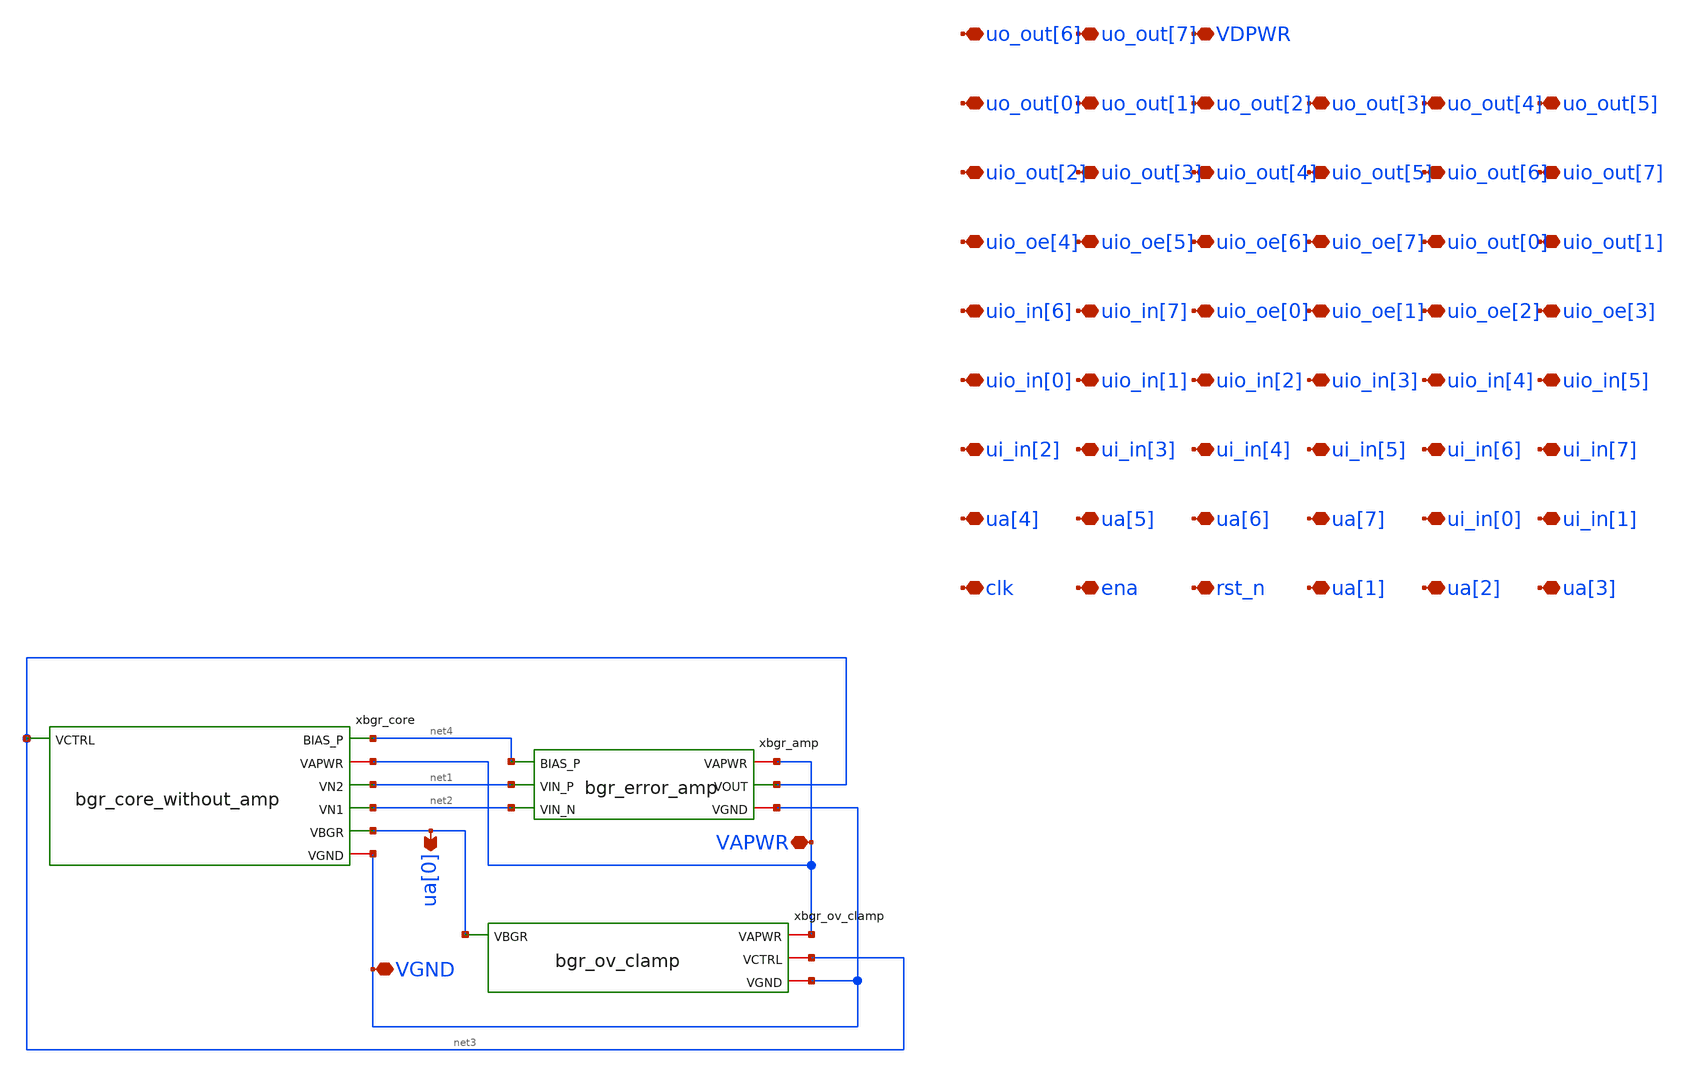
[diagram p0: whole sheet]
** sch_path: xschem/tt_um_rahulbhagwat_gf180_bandgap_reference.sch
**.subckt tt_um_rahulbhagwat_gf180_bandgap_reference VAPWR VGND ua[0] clk ena rst_n ua[1] ua[2]
*+ ua[3] ua[4] ua[5] ua[6] ua[7] ui_in[0] ui_in[1] ui_in[2] ui_in[3] ui_in[4] ui_in[5] ui_in[6] ui_in[7]
*+ uio_in[0] uio_in[1] uio_in[2] uio_in[3] uio_in[4] uio_in[5] uio_in[6] uio_in[7] uio_oe[0] uio_oe[1] uio_oe[2]
*+ uio_oe[3] uio_oe[4] uio_oe[5] uio_oe[6] uio_oe[7] uio_out[0] uio_out[1] uio_out[2] uio_out[3] uio_out[4]
*+ uio_out[5] uio_out[6] uio_out[7] uo_out[0] uo_out[1] uo_out[2] uo_out[3] uo_out[4] uo_out[5] uo_out[6]
*+ uo_out[7] VDPWR
*.iopin VAPWR
*.iopin VGND
*.opin ua[0]
*.iopin clk
*.iopin ena
*.iopin rst_n
*.iopin ua[1]
*.iopin ua[2]
*.iopin ua[3]
*.iopin ua[4]
*.iopin ua[5]
*.iopin ua[6]
*.iopin ua[7]
*.iopin ui_in[0]
*.iopin ui_in[1]
*.iopin ui_in[2]
*.iopin ui_in[3]
*.iopin ui_in[4]
*.iopin ui_in[5]
*.iopin ui_in[6]
*.iopin ui_in[7]
*.iopin uio_in[0]
*.iopin uio_in[1]
*.iopin uio_in[2]
*.iopin uio_in[3]
*.iopin uio_in[4]
*.iopin uio_in[5]
*.iopin uio_in[6]
*.iopin uio_in[7]
*.iopin uio_oe[0]
*.iopin uio_oe[1]
*.iopin uio_oe[2]
*.iopin uio_oe[3]
*.iopin uio_oe[4]
*.iopin uio_oe[5]
*.iopin uio_oe[6]
*.iopin uio_oe[7]
*.iopin uio_out[0]
*.iopin uio_out[1]
*.iopin uio_out[2]
*.iopin uio_out[3]
*.iopin uio_out[4]
*.iopin uio_out[5]
*.iopin uio_out[6]
*.iopin uio_out[7]
*.iopin uo_out[0]
*.iopin uo_out[1]
*.iopin uo_out[2]
*.iopin uo_out[3]
*.iopin uo_out[4]
*.iopin uo_out[5]
*.iopin uo_out[6]
*.iopin uo_out[7]
*.iopin VDPWR
xbgr_core net4 VAPWR net3 net1 net2 ua[0] VGND bgr_core_without_amp
xbgr_amp net4 VAPWR net1 net2 net3 VGND bgr_error_amp
xbgr_ov_clamp VAPWR ua[0] net3 VGND bgr_ov_clamp
**.ends

* expanding   symbol:  bgr_core_without_amp.sym # of pins=7
** sym_path: xschem/bgr_core_without_amp.sym
** sch_path: xschem/bgr_core_without_amp.sch
.subckt bgr_core_without_amp BIAS_P VAPWR VCTRL VN2 VN1 VBGR VGND
*.iopin VGND
*.iopin VAPWR
*.opin VBGR
*.ipin VCTRL
*.opin BIAS_P
*.opin VN1
*.opin VN2
XQ1 VN1 VBGR E1 VGND npn_05p00x05p00 m=1
XQ2 VN2 VBGR E2 VGND npn_05p00x05p00 m=8
XR1 E1 E2 VGND ppolyf_u_1k r_width=1.18e-6 r_length=3e-6 m=1
XR2 VGND E1 VGND ppolyf_u_1k r_width=1e-6 r_length=62.65e-6 m=1
XR3 VGND VBGR VGND ppolyf_u_1k r_width=1e-6 r_length=137e-6 m=1
XM1 VN2 VCTRL VAPWR VAPWR pfet_03v3 L=4u W=8u nf=1 ad='int((nf+1)/2) * W/nf * 0.18u' as='int((nf+2)/2) * W/nf * 0.18u'
+ pd='2*int((nf+1)/2) * (W/nf + 0.18u)' ps='2*int((nf+2)/2) * (W/nf + 0.18u)' nrd='0.18u / W' nrs='0.18u / W'
+ sa=0 sb=0 sd=0 m=1
XM2 VN1 VCTRL VAPWR VAPWR pfet_03v3 L=4u W=8u nf=1 ad='int((nf+1)/2) * W/nf * 0.18u' as='int((nf+2)/2) * W/nf * 0.18u'
+ pd='2*int((nf+1)/2) * (W/nf + 0.18u)' ps='2*int((nf+2)/2) * (W/nf + 0.18u)' nrd='0.18u / W' nrs='0.18u / W'
+ sa=0 sb=0 sd=0 m=1
XM3 NBIAS_N VCTRL VAPWR VAPWR pfet_03v3 L=4u W=2u nf=1 ad='int((nf+1)/2) * W/nf * 0.18u' as='int((nf+2)/2) * W/nf * 0.18u'
+ pd='2*int((nf+1)/2) * (W/nf + 0.18u)' ps='2*int((nf+2)/2) * (W/nf + 0.18u)' nrd='0.18u / W' nrs='0.18u / W'
+ sa=0 sb=0 sd=0 m=1
XM4 VBGR VCTRL VAPWR VAPWR pfet_03v3 L=4u W=64u nf=1 ad='int((nf+1)/2) * W/nf * 0.18u' as='int((nf+2)/2) * W/nf * 0.18u'
+ pd='2*int((nf+1)/2) * (W/nf + 0.18u)' ps='2*int((nf+2)/2) * (W/nf + 0.18u)' nrd='0.18u / W' nrs='0.18u / W'
+ sa=0 sb=0 sd=0 m=1
XM5 BIAS_P BIAS_P VAPWR VAPWR pfet_03v3 L=4u W=1u nf=1 ad='int((nf+1)/2) * W/nf * 0.18u' as='int((nf+2)/2) * W/nf * 0.18u'
+ pd='2*int((nf+1)/2) * (W/nf + 0.18u)' ps='2*int((nf+2)/2) * (W/nf + 0.18u)' nrd='0.18u / W' nrs='0.18u / W'
+ sa=0 sb=0 sd=0 m=1
XM6 BIAS_P NBIAS_N VGND VGND nfet_03v3 L=4u W=1u nf=1 ad='int((nf+1)/2) * W/nf * 0.18u' as='int((nf+2)/2) * W/nf * 0.18u'
+ pd='2*int((nf+1)/2) * (W/nf + 0.18u)' ps='2*int((nf+2)/2) * (W/nf + 0.18u)' nrd='0.18u / W' nrs='0.18u / W'
+ sa=0 sb=0 sd=0 m=1
XM7 NBIAS_N NBIAS_N VGND VGND nfet_03v3 L=4u W=1u nf=1 ad='int((nf+1)/2) * W/nf * 0.18u' as='int((nf+2)/2) * W/nf * 0.18u'
+ pd='2*int((nf+1)/2) * (W/nf + 0.18u)' ps='2*int((nf+2)/2) * (W/nf + 0.18u)' nrd='0.18u / W' nrs='0.18u / W'
+ sa=0 sb=0 sd=0 m=1
.ends


* expanding   symbol:  bgr_error_amp.sym # of pins=6
** sym_path: xschem/bgr_error_amp.sym
** sch_path: xschem/bgr_error_amp.sch
.subckt bgr_error_amp BIAS_P VAPWR VIN_P VIN_N VOUT VGND
*.ipin VIN_P
*.ipin VIN_N
*.ipin BIAS_P
*.iopin VAPWR
*.iopin VGND
*.opin VOUT
XMDIFF_P net1 VIN_P TAIL_P VAPWR pfet_03v3 L=0.28u W=0.22u nf=1 ad='int((nf+1)/2) * W/nf * 0.18u' as='int((nf+2)/2) * W/nf * 0.18u'
+ pd='2*int((nf+1)/2) * (W/nf + 0.18u)' ps='2*int((nf+2)/2) * (W/nf + 0.18u)' nrd='0.18u / W' nrs='0.18u / W'
+ sa=0 sb=0 sd=0 m=1
XMDIFF_N VOUT VIN_N TAIL_P VAPWR pfet_03v3 L=0.28u W=0.22u nf=1 ad='int((nf+1)/2) * W/nf * 0.18u' as='int((nf+2)/2) * W/nf * 0.18u'
+ pd='2*int((nf+1)/2) * (W/nf + 0.18u)' ps='2*int((nf+2)/2) * (W/nf + 0.18u)' nrd='0.18u / W' nrs='0.18u / W'
+ sa=0 sb=0 sd=0 m=1
XMTAIL TAIL_P BIAS_P VAPWR VAPWR pfet_03v3 L=0.28u W=0.22u nf=1 ad='int((nf+1)/2) * W/nf * 0.18u' as='int((nf+2)/2) * W/nf * 0.18u'
+ pd='2*int((nf+1)/2) * (W/nf + 0.18u)' ps='2*int((nf+2)/2) * (W/nf + 0.18u)' nrd='0.18u / W' nrs='0.18u / W'
+ sa=0 sb=0 sd=0 m=1
XMLOAD_REF net1 net1 VGND VGND nfet_03v3 L=0.28u W=0.22u nf=1 ad='int((nf+1)/2) * W/nf * 0.18u' as='int((nf+2)/2) * W/nf * 0.18u'
+ pd='2*int((nf+1)/2) * (W/nf + 0.18u)' ps='2*int((nf+2)/2) * (W/nf + 0.18u)' nrd='0.18u / W' nrs='0.18u / W'
+ sa=0 sb=0 sd=0 m=1
XMLOAD_OUT VOUT net1 VGND VGND nfet_03v3 L=0.28u W=0.22u nf=1 ad='int((nf+1)/2) * W/nf * 0.18u' as='int((nf+2)/2) * W/nf * 0.18u'
+ pd='2*int((nf+1)/2) * (W/nf + 0.18u)' ps='2*int((nf+2)/2) * (W/nf + 0.18u)' nrd='0.18u / W' nrs='0.18u / W'
+ sa=0 sb=0 sd=0 m=1
.ends


* expanding   symbol:  bgr_ov_clamp.sym # of pins=4
** sym_path: xschem/bgr_ov_clamp.sym
** sch_path: xschem/bgr_ov_clamp.sch
.subckt bgr_ov_clamp VAPWR VBGR VCTRL VGND
*.iopin VAPWR
*.iopin VGND
*.ipin VBGR
*.iopin VCTRL
XMOVDET_N OV_N VBGR VGND VGND nfet_03v3 L=1u W=0.3u nf=1 ad='int((nf+1)/2) * W/nf * 0.18u' as='int((nf+2)/2) * W/nf * 0.18u'
+ pd='2*int((nf+1)/2) * (W/nf + 0.18u)' ps='2*int((nf+2)/2) * (W/nf + 0.18u)' nrd='0.18u / W' nrs='0.18u / W'
+ sa=0 sb=0 sd=0 m=1
XMOVDET_P OV_N VBGR VAPWR VAPWR pfet_03v3 L=4u W=8u nf=1 ad='int((nf+1)/2) * W/nf * 0.18u' as='int((nf+2)/2) * W/nf * 0.18u'
+ pd='2*int((nf+1)/2) * (W/nf + 0.18u)' ps='2*int((nf+2)/2) * (W/nf + 0.18u)' nrd='0.18u / W' nrs='0.18u / W'
+ sa=0 sb=0 sd=0 m=1
XMOVCLAMP VCTRL OV_N VAPWR VAPWR pfet_03v3 L=8u W=0.5u nf=1 ad='int((nf+1)/2) * W/nf * 0.18u' as='int((nf+2)/2) * W/nf * 0.18u'
+ pd='2*int((nf+1)/2) * (W/nf + 0.18u)' ps='2*int((nf+2)/2) * (W/nf + 0.18u)' nrd='0.18u / W' nrs='0.18u / W'
+ sa=0 sb=0 sd=0 m=1
.ends

.end
